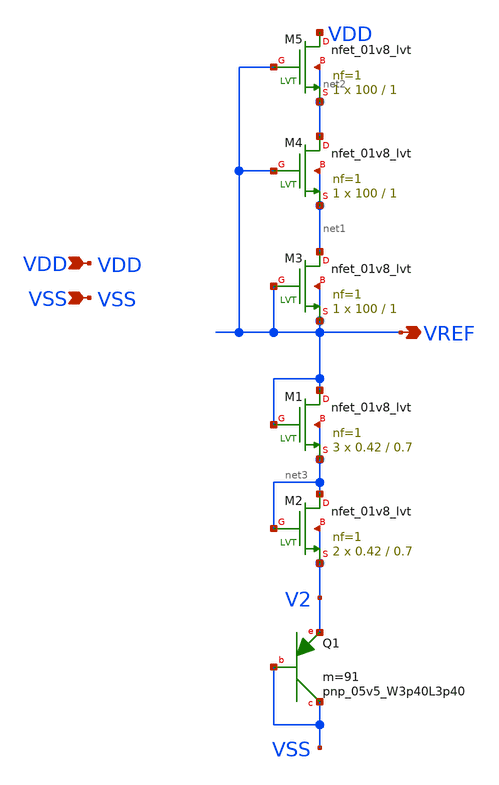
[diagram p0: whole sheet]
** sch_path: design/LELO_SVOD_SKY130A/LELO_SVOD_VTREF.sch
**.subckt LELO_SVOD_VTREF VDD VSS VREF
*.ipin VDD
*.ipin VSS
*.opin VREF
XQ1 VSS VSS V2 sky130_fd_pr__pnp_05v5_W3p40L3p40 m=91
XM1 VREF VREF net3 net3 sky130_fd_pr__nfet_01v8_lvt L=0.7 W=0.42 nf=1 ad='int((1 + 1)/2) * 0.42 / 1 * 0.29'
+ as='int((1 + 2)/2) * 0.42 / 1 * 0.29' pd='2*int((1 + 1)/2) * (0.42 / 1 + 0.29)' ps='2*int((1 + 2)/2) * (0.42 / 1 + 0.29)'
+ nrd='0.29 / 0.42 ' nrs='0.29 / 0.42 ' sa=0 sb=0 sd=0 mult=3 m=3
XM2 net3 net3 V2 V2 sky130_fd_pr__nfet_01v8_lvt L=0.7 W=0.42 nf=1 ad='int((1 + 1)/2) * 0.42 / 1 * 0.29'
+ as='int((1 + 2)/2) * 0.42 / 1 * 0.29' pd='2*int((1 + 1)/2) * (0.42 / 1 + 0.29)' ps='2*int((1 + 2)/2) * (0.42 / 1 + 0.29)'
+ nrd='0.29 / 0.42 ' nrs='0.29 / 0.42 ' sa=0 sb=0 sd=0 mult=2 m=2
XM3 net1 VREF VREF VREF sky130_fd_pr__nfet_01v8_lvt L=1 W=100 nf=1 ad='int((1 + 1)/2) * 100 / 1 * 0.29'
+ as='int((1 + 2)/2) * 100 / 1 * 0.29' pd='2*int((1 + 1)/2) * (100 / 1 + 0.29)' ps='2*int((1 + 2)/2) * (100 / 1 + 0.29)'
+ nrd='0.29 / 100 ' nrs='0.29 / 100 ' sa=0 sb=0 sd=0 mult=1 m=1
XM4 net2 VREF net1 net1 sky130_fd_pr__nfet_01v8_lvt L=1 W=100 nf=1 ad='int((1 + 1)/2) * 100 / 1 * 0.29'
+ as='int((1 + 2)/2) * 100 / 1 * 0.29' pd='2*int((1 + 1)/2) * (100 / 1 + 0.29)' ps='2*int((1 + 2)/2) * (100 / 1 + 0.29)'
+ nrd='0.29 / 100 ' nrs='0.29 / 100 ' sa=0 sb=0 sd=0 mult=1 m=1
XM5 VDD VREF net2 net2 sky130_fd_pr__nfet_01v8_lvt L=1 W=100 nf=1 ad='int((1 + 1)/2) * 100 / 1 * 0.29'
+ as='int((1 + 2)/2) * 100 / 1 * 0.29' pd='2*int((1 + 1)/2) * (100 / 1 + 0.29)' ps='2*int((1 + 2)/2) * (100 / 1 + 0.29)'
+ nrd='0.29 / 100 ' nrs='0.29 / 100 ' sa=0 sb=0 sd=0 mult=1 m=1
**.ends
.end
